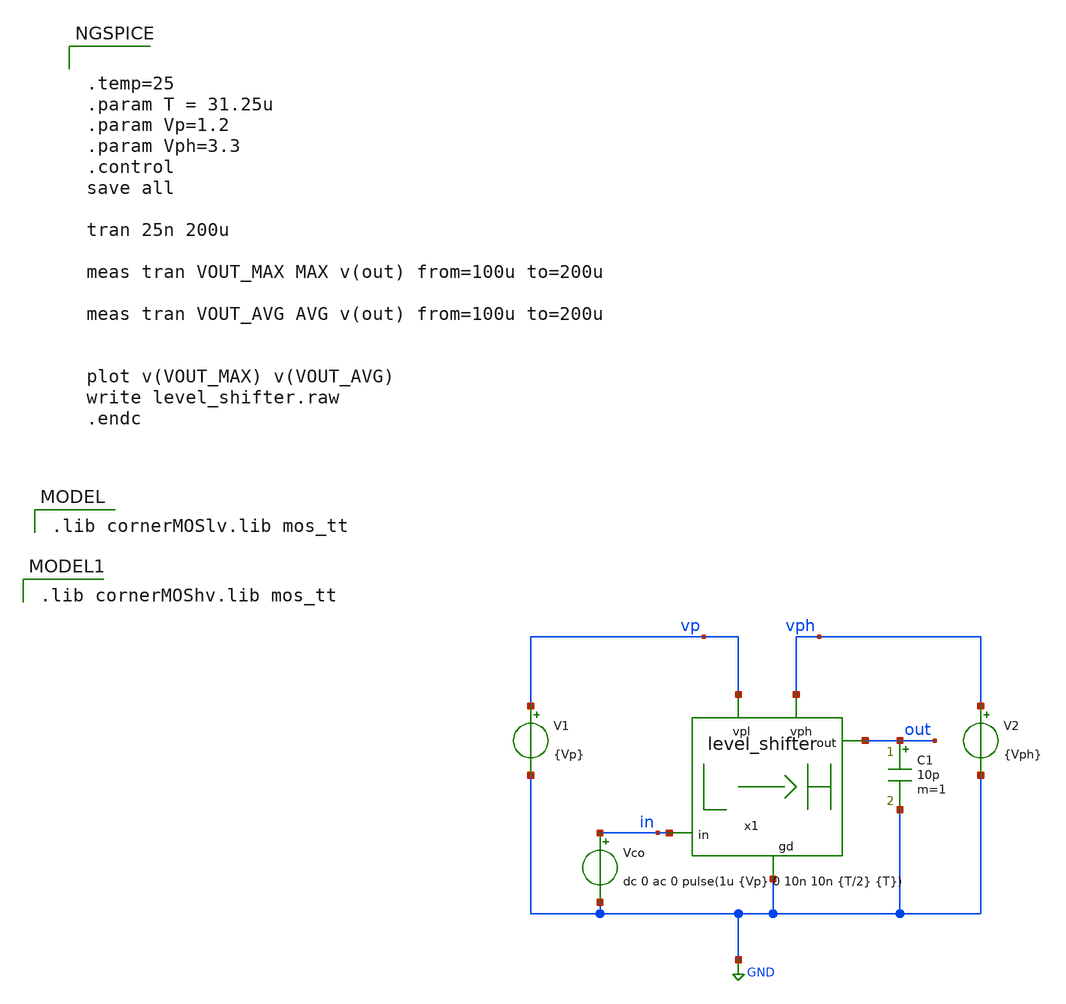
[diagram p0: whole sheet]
** sch_path: schematics/misc/level_shifter_tb.sch
**.subckt level_shifter_tb
x1 vph out vp in GND level_shifter
V1 vp GND {Vp}
V2 vph GND {Vph}
C1 out GND 10p m=1
Vco in GND dc 0 ac 0 pulse(1u {Vp} 0 10n 10n {T/2} {T})
**** begin user architecture code
 .lib cornerMOSlv.lib mos_tt



.temp=25
.param T = 31.25u
.param Vp=1.2
.param Vph=3.3
.control
save all

tran 25n 200u

meas tran VOUT_MAX MAX v(out) from=100u to=200u

meas tran VOUT_AVG AVG v(out) from=100u to=200u


plot v(VOUT_MAX) v(VOUT_AVG)
write level_shifter.raw
.endc


 .lib cornerMOShv.lib mos_tt

**** end user architecture code
**.ends

* expanding   symbol:  level_shifter.sym # of pins=5
** sym_path: schematics/misc/level_shifter.sym
** sch_path: schematics/misc/level_shifter.sch
.subckt level_shifter vph out vpl in gd
*.ipin in
*.opin out
*.ipin gd
*.ipin vph
*.ipin vpl
XM16 4 1_stage_out gd gd sg13_hv_nmos w=2u l=0.45u ng=1 m=1 mm_ok=1
XM8 3_stage_out 2_stage_out gd gd sg13_hv_nmos w=4u l=0.45u ng=1 m=1 mm_ok=1
XM12 net5 3_stage_out gd gd sg13_hv_nmos w=1u l=0.45u ng=1 m=1 mm_ok=1
XM13 out 3_stage_out net5 gd sg13_hv_nmos w=1u l=0.45u ng=1 m=1 mm_ok=1
XM14 4 1_stage_out net2 vph sg13_hv_pmos w=1u l=0.4u ng=1 m=1 mm_ok=1
XM9 3_stage_out 2_stage_out net3 vph sg13_hv_pmos w=2u l=0.4u ng=1 m=1 mm_ok=1
XM10 out 3_stage_out vph vph sg13_hv_pmos w=2u l=0.4u ng=1 m=1 mm_ok=1
XM11 net3 4 vph vph sg13_hv_pmos w=2u l=0.4u ng=1 m=1 mm_ok=1
XM7 net2 3_stage_out vph vph sg13_hv_pmos w=1u l=0.4u ng=1 m=1 mm_ok=1
XM3 1_stage_out in net1 gd sg13_lv_nmos w=1u l=0.13u ng=1 m=1 mm_ok=1
XM4 net1 in gd gd sg13_lv_nmos w=1u l=0.13u ng=1 m=1 mm_ok=1
XM5 net4 1_stage_out gd gd sg13_lv_nmos w=1u l=0.13u ng=1 m=1 mm_ok=1
XM6 2_stage_out 1_stage_out net4 gd sg13_lv_nmos w=1u l=0.13u ng=1 m=1 mm_ok=1
XM15 2_stage_out 1_stage_out vpl vpl sg13_lv_pmos w=2u l=0.13u ng=1 m=1 mm_ok=1
XM1 1_stage_out in vpl vpl sg13_lv_pmos w=2u l=0.13u ng=1 m=1 mm_ok=1
.ends

.GLOBAL GND
.end
